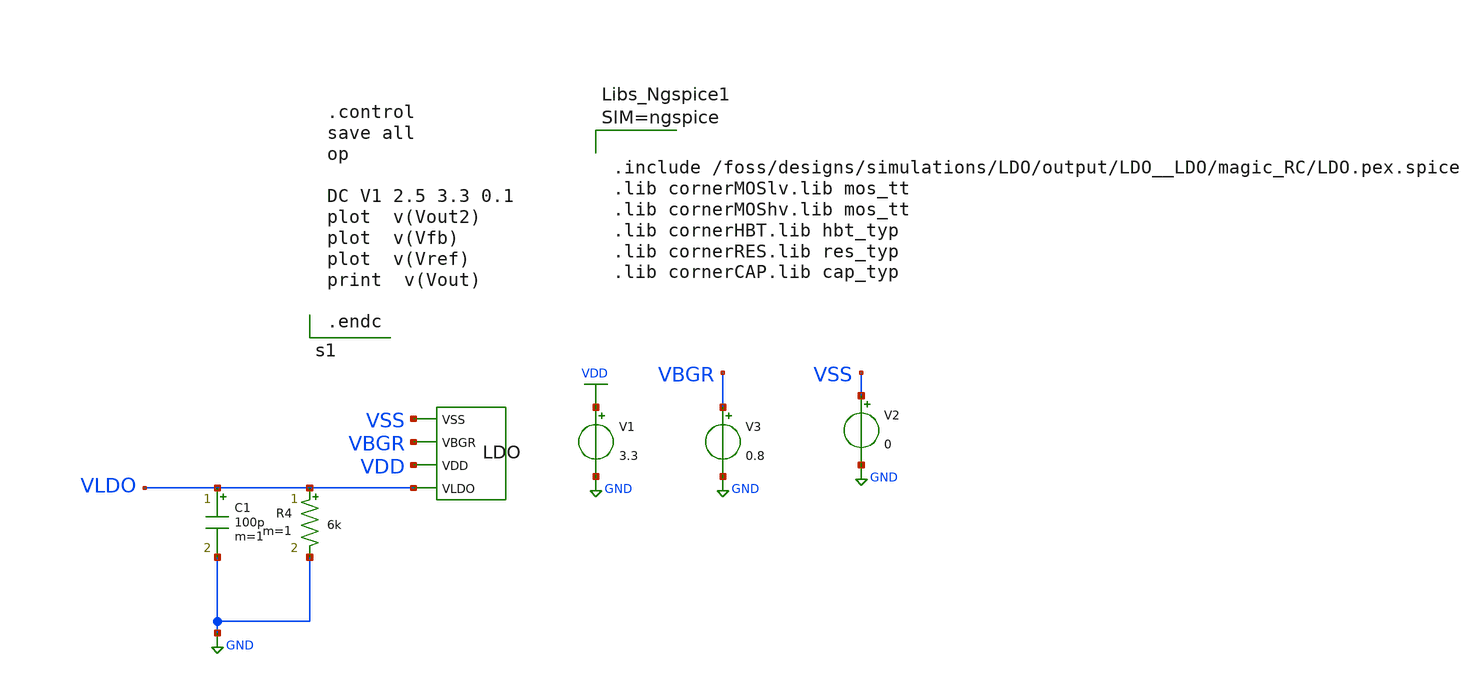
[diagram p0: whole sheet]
** sch_path: dependencies/LDO/LDO-main/testbenches/line-regulation/ldo_post_layout_sim_dc_LinearRegulation.sch
**.subckt ldo_post_layout_sim_dc_LinearRegulation
V1 VDD GND 3.3
V3 VBGR GND 0.8
V2 VSS GND 0
X1 VSS VBGR VDD VLDO LDO
C1 VLDO GND 100p m=1
R4 VLDO GND 6k m=1
**** begin user architecture code



.include /foss/designs/simulations/LDO/output/LDO__LDO/magic_RC/LDO.pex.spice
.lib cornerMOSlv.lib mos_tt
.lib cornerMOShv.lib mos_tt
.lib cornerHBT.lib hbt_typ
.lib cornerRES.lib res_typ
.lib cornerCAP.lib cap_typ





.control
save all
op

DC V1 2.5 3.3 0.1
plot  v(Vout2)
plot  v(Vfb)
plot  v(Vref)
print  v(Vout)

.endc

**** end user architecture code
**.ends
.GLOBAL GND
.GLOBAL VDD
.end
